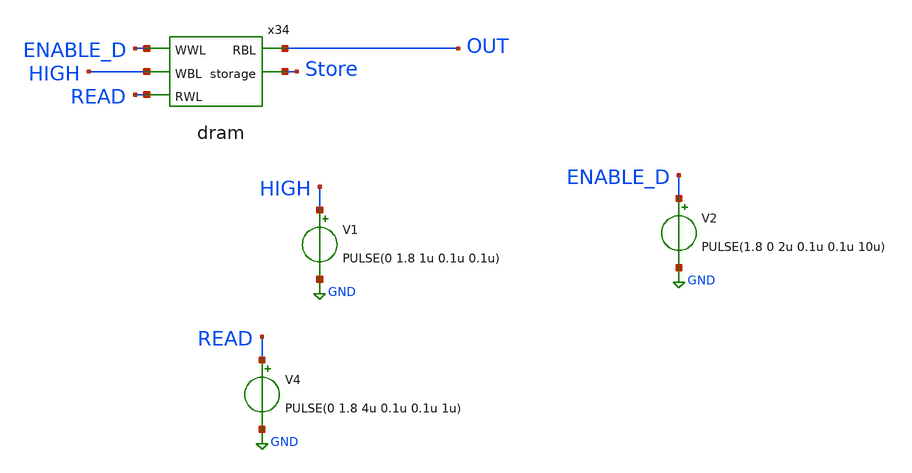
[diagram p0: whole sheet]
** sch_path: xschem/testbench/dram_tb.sch
**.subckt dram_tb
x34 ENABLE_D OUT Store HIGH READ dram
V1 HIGH GND PULSE(0 1.8 1u 0.1u 0.1u)
V2 ENABLE_D GND PULSE(1.8 0 2u 0.1u 0.1u 10u)
V4 READ GND PULSE(0 1.8 4u 0.1u 0.1u 1u)
**** begin user architecture code

** opencircuitdesign pdks install
.lib $::SKYWATER_MODELS/sky130.lib.spice tt


**** end user architecture code
**.ends

* expanding   symbol:  digital_prims/dram.sym # of pins=5
** sym_path: xschem/digital_prims/dram.sym
** sch_path: xschem/digital_prims/dram.sch
.subckt dram WWL RBL storage WBL RWL
*.opin RBL
*.ipin RWL
*.ipin WBL
*.ipin WWL
*.opin storage
XM3 RWL storage RBL GND sky130_fd_pr__nfet_01v8 L=0.15 W=1 nf=1 ad='int((nf+1)/2) * W/nf * 0.29' as='int((nf+2)/2) * W/nf * 0.29'
+ pd='2*int((nf+1)/2) * (W/nf + 0.29)' ps='2*int((nf+2)/2) * (W/nf + 0.29)' nrd='0.29 / W' nrs='0.29 / W'
+ sa=0 sb=0 sd=0 mult=1 m=1
XM1 WBL WWL storage GND sky130_fd_pr__nfet_01v8 L=0.15 W=1 nf=1 ad='int((nf+1)/2) * W/nf * 0.29' as='int((nf+2)/2) * W/nf * 0.29'
+ pd='2*int((nf+1)/2) * (W/nf + 0.29)' ps='2*int((nf+2)/2) * (W/nf + 0.29)' nrd='0.29 / W' nrs='0.29 / W'
+ sa=0 sb=0 sd=0 mult=1 m=1
.ends

.GLOBAL GND
**** begin user architecture code


.control
*dc v2 0 1.8 0.05
*plot v(test)
tran 0.1u 20u
plot v(Store) v(read) v(OUT)
write adc_testbench.raw
options filetype=ascii
write adc_testbench.out
.endc


**** end user architecture code
.end
